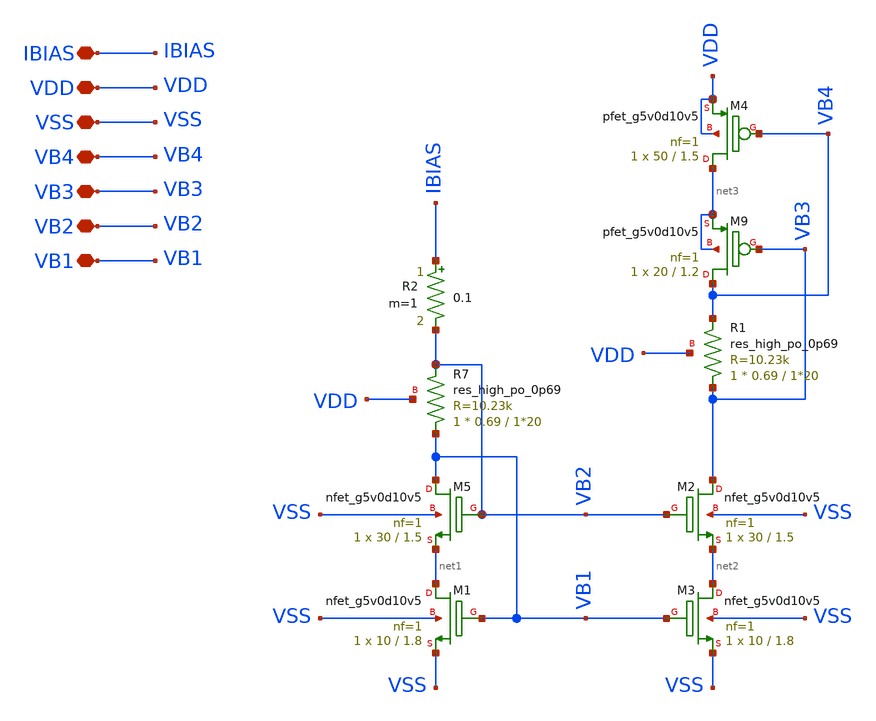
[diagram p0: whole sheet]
** sch_path: folded_cascode_amplifier/Low_voltage_current_mirror_NMOS/bias_generator.sch
**.subckt bias_generator IBIAS VDD VB4 VB3 VB2 VB1 VSS
*.iopin IBIAS
*.iopin VDD
*.iopin VB4
*.iopin VB3
*.iopin VB2
*.iopin VB1
*.iopin VSS
XM5 VB1 VB2 net1 VSS sky130_fd_pr__nfet_g5v0d10v5 L=1.5 W=30 nf=1 ad='int((1 + 1)/2) * 30 / 1 * 0.29'
+ as='int((1 + 2)/2) * 30 / 1 * 0.29' pd='2*int((1 + 1)/2) * (30 / 1 + 0.29)' ps='2*int((1 + 2)/2) * (30 / 1 + 0.29)'
+ nrd='0.29 / 30 ' nrs='0.29 / 30 ' sa=0 sb=0 sd=0 mult=1 m=1
XM1 net1 VB1 VSS VSS sky130_fd_pr__nfet_g5v0d10v5 L=1.8 W=10 nf=1 ad='int((1 + 1)/2) * 10 / 1 * 0.29'
+ as='int((1 + 2)/2) * 10 / 1 * 0.29' pd='2*int((1 + 1)/2) * (10 / 1 + 0.29)' ps='2*int((1 + 2)/2) * (10 / 1 + 0.29)'
+ nrd='0.29 / 10 ' nrs='0.29 / 10 ' sa=0 sb=0 sd=0 mult=1 m=1
XR7 VB1 VB2 VDD sky130_fd_pr__res_high_po_0p69 L=1*20 mult=1 m=1
XM2 VB3 VB2 net2 VSS sky130_fd_pr__nfet_g5v0d10v5 L=1.5 W=30 nf=1 ad='int((1 + 1)/2) * 30 / 1 * 0.29'
+ as='int((1 + 2)/2) * 30 / 1 * 0.29' pd='2*int((1 + 1)/2) * (30 / 1 + 0.29)' ps='2*int((1 + 2)/2) * (30 / 1 + 0.29)'
+ nrd='0.29 / 30 ' nrs='0.29 / 30 ' sa=0 sb=0 sd=0 mult=1 m=1
XM3 net2 VB1 VSS VSS sky130_fd_pr__nfet_g5v0d10v5 L=1.8 W=10 nf=1 ad='int((1 + 1)/2) * 10 / 1 * 0.29'
+ as='int((1 + 2)/2) * 10 / 1 * 0.29' pd='2*int((1 + 1)/2) * (10 / 1 + 0.29)' ps='2*int((1 + 2)/2) * (10 / 1 + 0.29)'
+ nrd='0.29 / 10 ' nrs='0.29 / 10 ' sa=0 sb=0 sd=0 mult=1 m=1
XR1 VB3 VB4 VDD sky130_fd_pr__res_high_po_0p69 L=1*20 mult=1 m=1
XM9 VB4 VB3 net3 net3 sky130_fd_pr__pfet_g5v0d10v5 L=1.2 W=20 nf=1 ad='int((1 + 1)/2) * 20 / 1 * 0.29'
+ as='int((1 + 2)/2) * 20 / 1 * 0.29' pd='2*int((1 + 1)/2) * (20 / 1 + 0.29)' ps='2*int((1 + 2)/2) * (20 / 1 + 0.29)'
+ nrd='0.29 / 20 ' nrs='0.29 / 20 ' sa=0 sb=0 sd=0 mult=1 m=1
XM4 net3 VB4 VDD VDD sky130_fd_pr__pfet_g5v0d10v5 L=1.5 W=50 nf=1 ad='int((1 + 1)/2) * 50 / 1 * 0.29'
+ as='int((1 + 2)/2) * 50 / 1 * 0.29' pd='2*int((1 + 1)/2) * (50 / 1 + 0.29)' ps='2*int((1 + 2)/2) * (50 / 1 + 0.29)'
+ nrd='0.29 / 50 ' nrs='0.29 / 50 ' sa=0 sb=0 sd=0 mult=1 m=1
R2 IBIAS VB2 0.1 m=1
**.ends
.end
